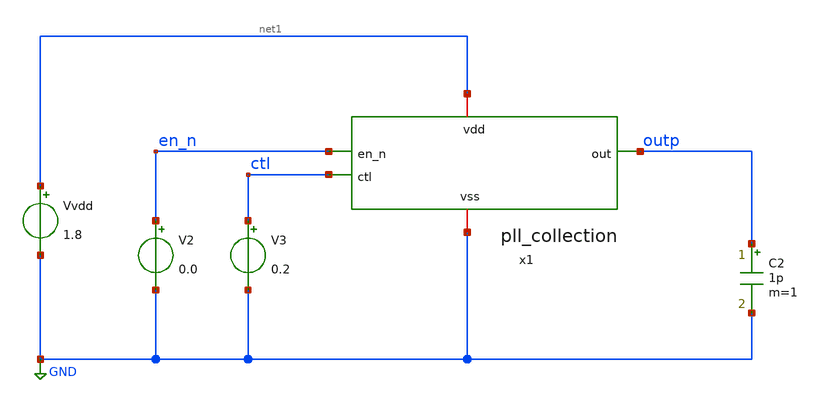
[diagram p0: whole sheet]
** sch_path: xschem/pll_collection/test/pll_collection_tb.sch
**.subckt pll_collection_tb
x1 net1 en_n ctl outp GND pll_collection
Vvdd net1 GND 1.8
V2 en_n GND 0.0
V3 ctl GND 0.2
C2 outp GND 1p m=1
**** begin user architecture code


.param temp=27
.temp 27

*.save v(ip) v(in) v(vctl) i(vdd)

.include sky130_fd_pr/cells/rf_nfet_01v8_lvt/sky130_fd_pr__rf_nfet_01v8_lvt_aM04W5p00L0p15.spice
.include sky130_fd_pr/cells/rf_nfet_01v8_lvt/sky130_fd_pr__rf_nfet_01v8_lvt_aM02W3p00L0p15.spice
.include sky130_fd_pr/cells/rf_nfet_01v8_lvt/sky130_fd_pr__rf_nfet_01v8_lvt_aM02W1p65L0p15.spice

.include sky130_fd_pr/cells/rf_pfet_01v8_lvt/sky130_fd_pr__rf_pfet_01v8_lvt_aM04W5p00L0p35.spice
.include sky130_fd_pr/cells/rf_pfet_01v8_lvt/sky130_fd_pr__rf_pfet_01v8_lvt_aM04W3p00L0p35.spice
.include sky130_fd_pr/cells/rf_pfet_01v8_lvt/sky130_fd_pr__rf_pfet_01v8_lvt_aM04W5p00L0p35.spice
.include sky130_fd_pr/cells/rf_pfet_01v8_lvt/sky130_fd_pr__rf_pfet_01v8_lvt_aM04W5p00L0p50.spice
.include sky130_fd_pr/cells/rf_pfet_01v8_lvt/sky130_fd_pr__rf_pfet_01v8_lvt_aM02W3p00L0p35.spice
.include sky130_fd_pr/cells/rf_pfet_01v8_lvt/sky130_fd_pr__rf_pfet_01v8_lvt_aM02W5p00L0p35.spice

.include sky130_fd_pr/cells/rf_pfet_01v8/sky130_fd_pr__rf_pfet_01v8_aM02W1p65L0p15.spice
.include sky130_fd_pr/cells/rf_pfet_01v8/sky130_fd_pr__rf_pfet_01v8_aM02W3p00L0p15.spice
.include sky130_fd_pr/cells/rf_pfet_01v8/sky130_fd_pr__rf_pfet_01v8_aM02W5p00L0p15.spice
.include sky130_fd_pr/cells/rf_pfet_01v8/sky130_fd_pr__rf_pfet_01v8_aM02W3p00L0p25.spice
.include sky130_fd_pr/cells/rf_pfet_01v8/sky130_fd_pr__rf_pfet_01v8_aM02W5p00L0p25.spice
.include sky130_fd_pr/cells/rf_pfet_01v8/sky130_fd_pr__rf_pfet_01v8_aF04W2p00L0p15.spice
.include sky130_fd_pr/cells/rf_pfet_01v8/sky130_fd_pr__rf_pfet_01v8_aF04W3p00L0p15.spice
.include sky130_fd_pr/cells/rf_pfet_01v8/sky130_fd_pr__rf_pfet_01v8_aM02W1p65L0p25.spice

.include sky130_fd_pr/cells/rf_nfet_01v8_lvt/sky130_fd_pr__rf_nfet_01v8_lvt_aF06W3p00L0p15.spice
.include sky130_fd_pr/cells/rf_nfet_01v8_lvt/sky130_fd_pr__rf_nfet_01v8_lvt_aF06W1p65L0p15.spice
.include sky130_fd_pr/cells/rf_nfet_01v8_lvt/sky130_fd_pr__rf_nfet_01v8_lvt_aF04W1p65L0p15.spice
.include sky130_fd_pr/cells/rf_nfet_01v8_lvt/sky130_fd_pr__rf_nfet_01v8_lvt_aF02W1p65L0p15.spice
.include sky130_fd_pr/cells/rf_nfet_01v8_lvt/sky130_fd_pr__rf_nfet_01v8_lvt_aF02W0p84L0p15.spice


.lib sky130_fd_pr/models/sky130.lib.spice tt
*.include sky130_fd_pr/models/corners/tt.spice


.tran 0.01n 1000n uic
.param vdd=1.8
.param vctl=0.2


**** end user architecture code
**.ends
.GLOBAL GND
**** begin user architecture code

**** end user architecture code
.end
